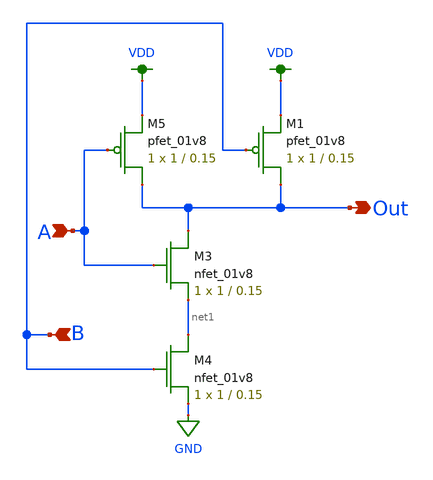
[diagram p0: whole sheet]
** sch_path: miniproject1/MP1_nand.sch
**.subckt MP1_nand A B Out
*.ipin A
*.ipin B
*.opin Out
XM3 Out A net1 GND sky130_fd_pr__nfet_01v8 L=0.15 W=1 nf=1 ad='int((nf+1)/2) * W/nf * 0.29' as='int((nf+2)/2) * W/nf * 0.29'
+ pd='2*int((nf+1)/2) * (W/nf + 0.29)' ps='2*int((nf+2)/2) * (W/nf + 0.29)' nrd='0.29 / W' nrs='0.29 / W'
+ sa=0 sb=0 sd=0 mult=1 m=1
XM4 net1 B GND GND sky130_fd_pr__nfet_01v8 L=0.15 W=1 nf=1 ad='int((nf+1)/2) * W/nf * 0.29' as='int((nf+2)/2) * W/nf * 0.29'
+ pd='2*int((nf+1)/2) * (W/nf + 0.29)' ps='2*int((nf+2)/2) * (W/nf + 0.29)' nrd='0.29 / W' nrs='0.29 / W'
+ sa=0 sb=0 sd=0 mult=1 m=1
XM1 Out B VDD VDD sky130_fd_pr__pfet_01v8 L=0.15 W=1 nf=1 ad='int((nf+1)/2) * W/nf * 0.29' as='int((nf+2)/2) * W/nf * 0.29'
+ pd='2*int((nf+1)/2) * (W/nf + 0.29)' ps='2*int((nf+2)/2) * (W/nf + 0.29)' nrd='0.29 / W' nrs='0.29 / W'
+ sa=0 sb=0 sd=0 mult=1 m=1
XM5 Out A VDD VDD sky130_fd_pr__pfet_01v8 L=0.15 W=1 nf=1 ad='int((nf+1)/2) * W/nf * 0.29' as='int((nf+2)/2) * W/nf * 0.29'
+ pd='2*int((nf+1)/2) * (W/nf + 0.29)' ps='2*int((nf+2)/2) * (W/nf + 0.29)' nrd='0.29 / W' nrs='0.29 / W'
+ sa=0 sb=0 sd=0 mult=1 m=1
**.ends
.GLOBAL VDD
.GLOBAL GND
.end
